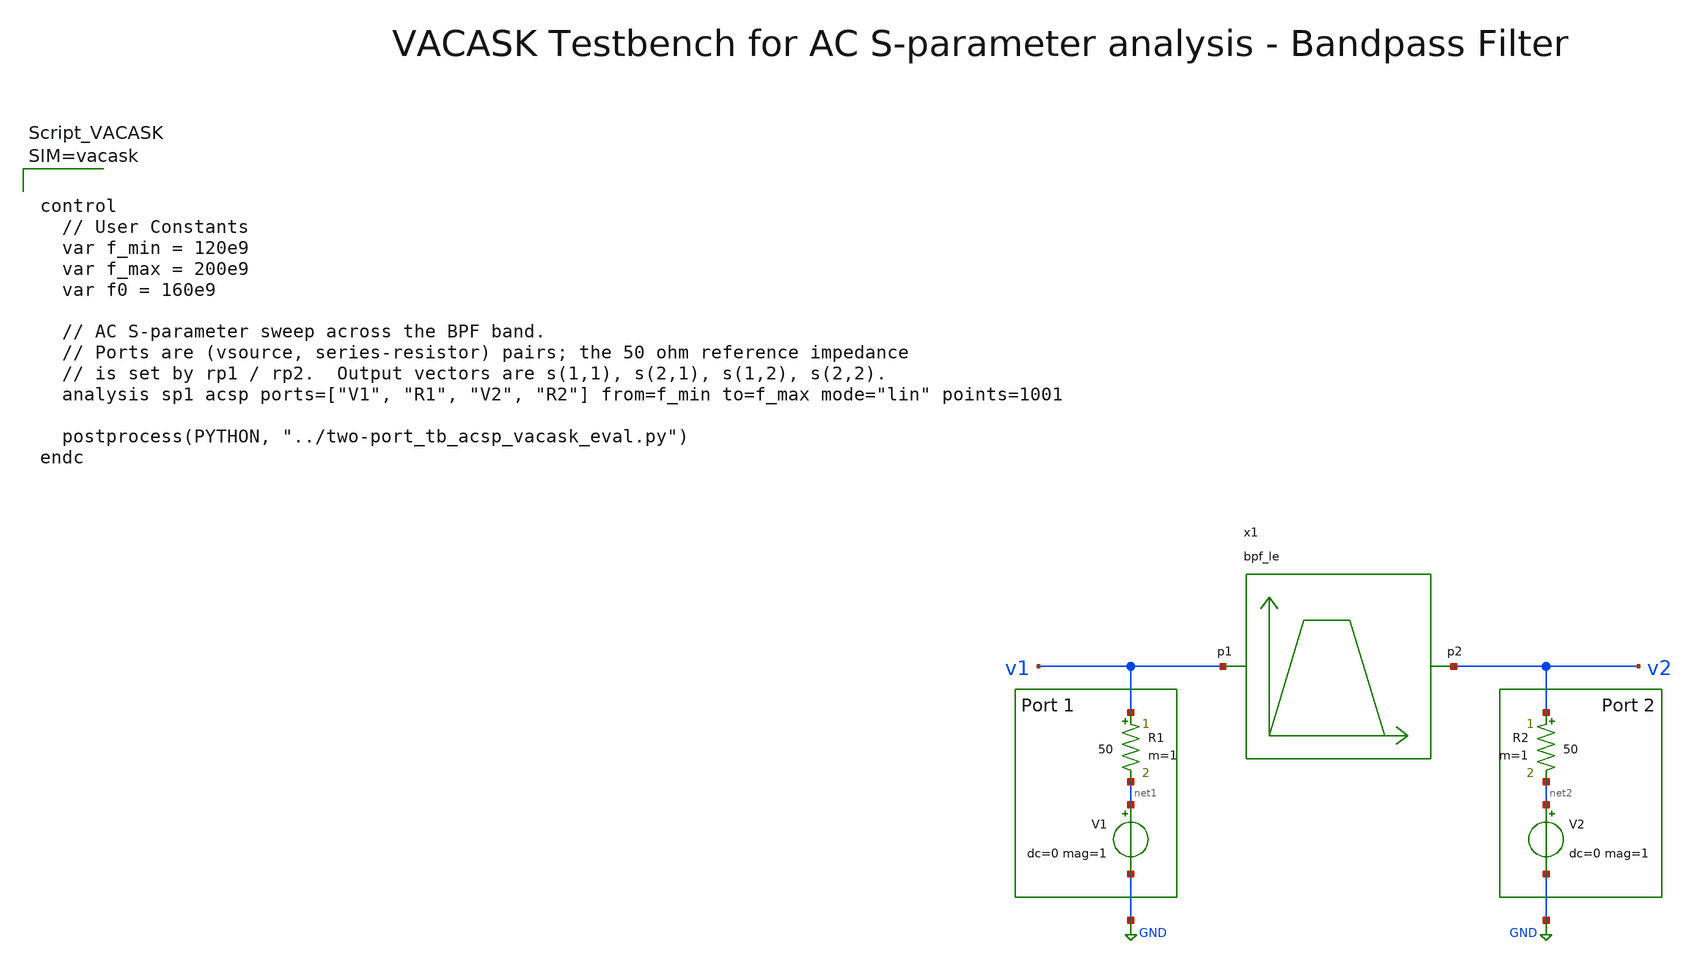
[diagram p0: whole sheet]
** sch_path: testbenches/xschem/two_port_tb_acsp_vacask.sch
**.subckt two_port_tb_acsp_vacask
x1 v1 v2 bpf_le
R1 v1 net1 50 m=1
V1 net1 GND dc=0 mag=1
R2 v2 net2 50 m=1
V2 net2 GND dc=0 mag=1
**** begin user architecture code






**** end user architecture code
**.ends
.GLOBAL GND
.end
